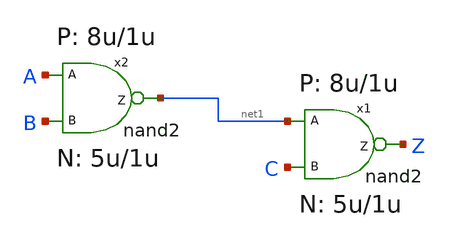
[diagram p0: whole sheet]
** sch_path: xschem_library/examples/test2.sch
**.subckt test2
x1 Z net1 C nand2 W_P=8u L_P=1u W_N=5u L_N=1u
x2 net1 A B nand2 W_P=8u L_P=1u W_N=5u L_N=1u
**.ends

* expanding   symbol:  nand2.sym # of pins=3
** sym_path: xschem_library/examples/nand2.sym
** sch_path: xschem_library/examples/nand2.sch
.subckt nand2 Z A B  W_P=8u L_P=1u W_N=5u L_N=1u
*.ipin A
*.opin Z
*.ipin B
m1 Z A net1 VSS nmos w=WN l=LN m=1
m2 Z B VCC VCC pmos w=WP l=LP m=1
m3 Z A VCC VCC pmos w=WP l=LP m=1
m4 net1 B VSS VSS nmos w=WN l=LN m=1
.ends

.GLOBAL VCC
.GLOBAL VSS
.end
